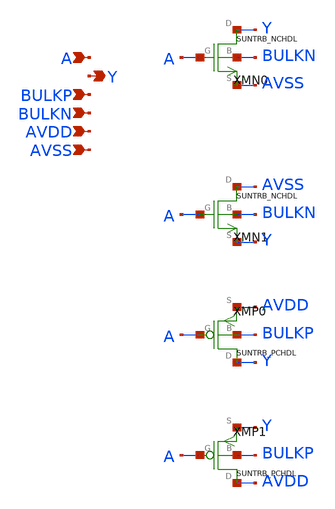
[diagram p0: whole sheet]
** sch_path: ip/sun_trb_sky130nm/design/SUN_TRB_SKY130NM/SUNTRB_IVX2_CV.sch
**.subckt SUNTRB_IVX2_CV A Y BULKP BULKN AVDD AVSS
*.ipin A
*.opin Y
*.ipin BULKP
*.ipin BULKN
*.ipin AVDD
*.ipin AVSS
XMN0 Y A AVSS BULKN SUNTRB_NCHDL xoffset=0 yoffset=0 angle=0
XMN1 AVSS A Y BULKN SUNTRB_NCHDL xoffset=0 yoffset=0 angle=0
XMP0 Y A AVDD BULKP SUNTRB_PCHDL xoffset=0 yoffset=0 angle=0
XMP1 AVDD A Y BULKP SUNTRB_PCHDL xoffset=0 yoffset=0 angle=0
**.ends
.end
